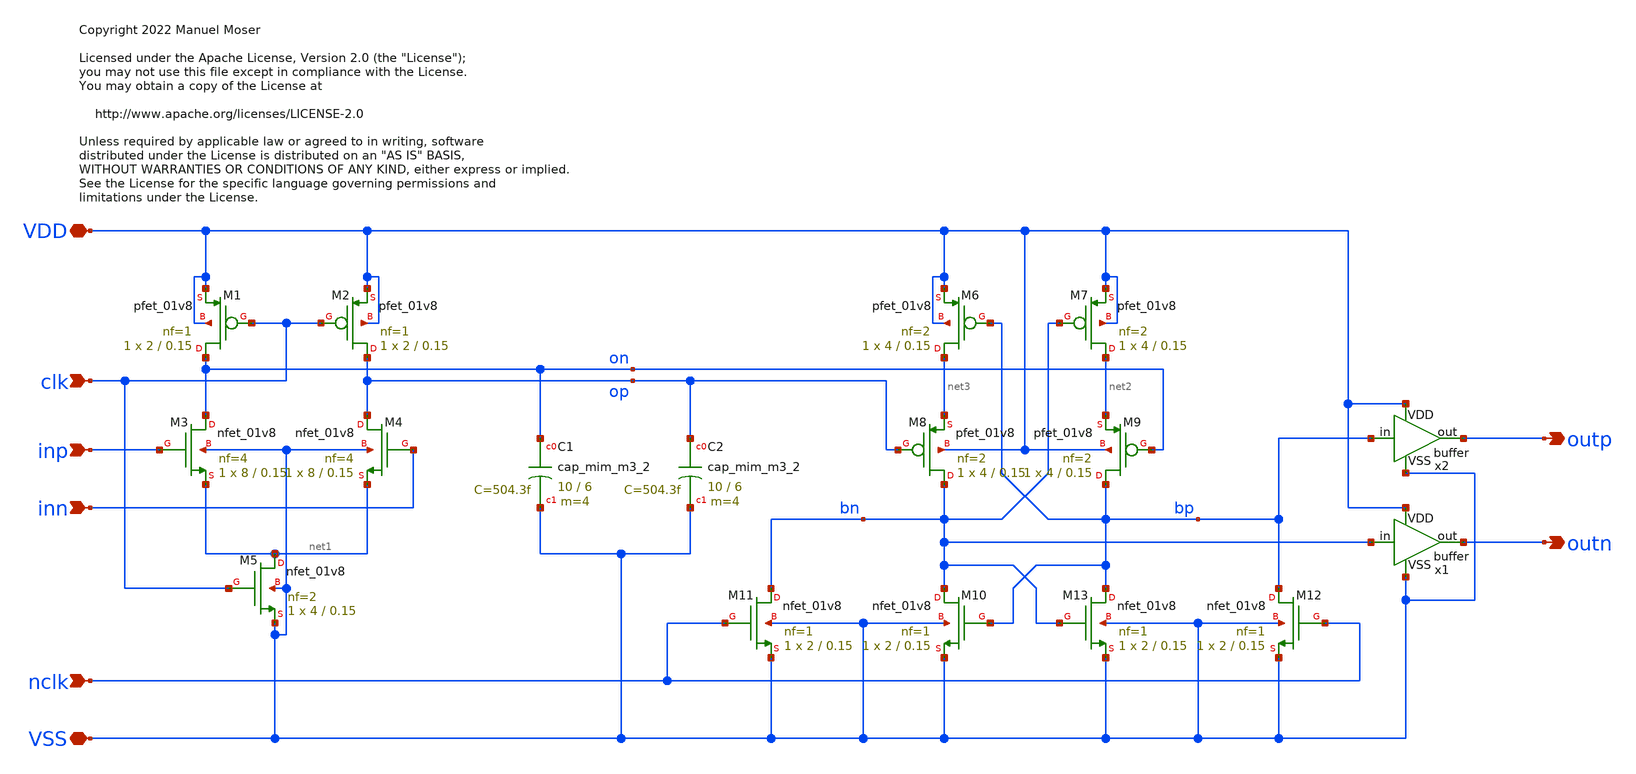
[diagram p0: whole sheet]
** sch_path: xschem/adc_comp_circuit/adc_comp_circuit.sch
* Copyright 2022 Manuel Moser
* Licensed under the Apache License, Version 2.0 (the "License");
**.subckt adc_comp_circuit VDD VSS inp inn clk nclk outp outn
*.iopin VDD
*.iopin VSS
*.ipin inp
*.ipin inn
*.ipin clk
*.ipin nclk
*.opin outp
*.opin outn
XM1 on clk VDD VDD sky130_fd_pr__pfet_01v8 L=0.15 W=2 nf=1 ad='int((nf+1)/2) * W/nf * 0.29' as='int((nf+2)/2) * W/nf * 0.29'
+ pd='2*int((nf+1)/2) * (W/nf + 0.29)' ps='2*int((nf+2)/2) * (W/nf + 0.29)' nrd='0.29 / W' nrs='0.29 / W'
+ sa=0 sb=0 sd=0 mult=1 m=1
XM2 op clk VDD VDD sky130_fd_pr__pfet_01v8 L=0.15 W=2 nf=1 ad='int((nf+1)/2) * W/nf * 0.29' as='int((nf+2)/2) * W/nf * 0.29'
+ pd='2*int((nf+1)/2) * (W/nf + 0.29)' ps='2*int((nf+2)/2) * (W/nf + 0.29)' nrd='0.29 / W' nrs='0.29 / W'
+ sa=0 sb=0 sd=0 mult=1 m=1
XM3 on inp net1 VSS sky130_fd_pr__nfet_01v8 L=0.15 W=8 nf=4 ad='int((nf+1)/2) * W/nf * 0.29' as='int((nf+2)/2) * W/nf * 0.29'
+ pd='2*int((nf+1)/2) * (W/nf + 0.29)' ps='2*int((nf+2)/2) * (W/nf + 0.29)' nrd='0.29 / W' nrs='0.29 / W'
+ sa=0 sb=0 sd=0 mult=1 m=1
XM4 op inn net1 VSS sky130_fd_pr__nfet_01v8 L=0.15 W=8 nf=4 ad='int((nf+1)/2) * W/nf * 0.29' as='int((nf+2)/2) * W/nf * 0.29'
+ pd='2*int((nf+1)/2) * (W/nf + 0.29)' ps='2*int((nf+2)/2) * (W/nf + 0.29)' nrd='0.29 / W' nrs='0.29 / W'
+ sa=0 sb=0 sd=0 mult=1 m=1
XM5 net1 clk VSS VSS sky130_fd_pr__nfet_01v8 L=0.15 W=4 nf=2 ad='int((nf+1)/2) * W/nf * 0.29' as='int((nf+2)/2) * W/nf * 0.29'
+ pd='2*int((nf+1)/2) * (W/nf + 0.29)' ps='2*int((nf+2)/2) * (W/nf + 0.29)' nrd='0.29 / W' nrs='0.29 / W'
+ sa=0 sb=0 sd=0 mult=1 m=1
XM6 net3 bp VDD VDD sky130_fd_pr__pfet_01v8 L=0.15 W=4 nf=2 ad='int((nf+1)/2) * W/nf * 0.29' as='int((nf+2)/2) * W/nf * 0.29'
+ pd='2*int((nf+1)/2) * (W/nf + 0.29)' ps='2*int((nf+2)/2) * (W/nf + 0.29)' nrd='0.29 / W' nrs='0.29 / W'
+ sa=0 sb=0 sd=0 mult=1 m=1
XM7 net2 bn VDD VDD sky130_fd_pr__pfet_01v8 L=0.15 W=4 nf=2 ad='int((nf+1)/2) * W/nf * 0.29' as='int((nf+2)/2) * W/nf * 0.29'
+ pd='2*int((nf+1)/2) * (W/nf + 0.29)' ps='2*int((nf+2)/2) * (W/nf + 0.29)' nrd='0.29 / W' nrs='0.29 / W'
+ sa=0 sb=0 sd=0 mult=1 m=1
XM8 bn op net3 VDD sky130_fd_pr__pfet_01v8 L=0.15 W=4 nf=2 ad='int((nf+1)/2) * W/nf * 0.29' as='int((nf+2)/2) * W/nf * 0.29'
+ pd='2*int((nf+1)/2) * (W/nf + 0.29)' ps='2*int((nf+2)/2) * (W/nf + 0.29)' nrd='0.29 / W' nrs='0.29 / W'
+ sa=0 sb=0 sd=0 mult=1 m=1
XM9 bp on net2 VDD sky130_fd_pr__pfet_01v8 L=0.15 W=4 nf=2 ad='int((nf+1)/2) * W/nf * 0.29' as='int((nf+2)/2) * W/nf * 0.29'
+ pd='2*int((nf+1)/2) * (W/nf + 0.29)' ps='2*int((nf+2)/2) * (W/nf + 0.29)' nrd='0.29 / W' nrs='0.29 / W'
+ sa=0 sb=0 sd=0 mult=1 m=1
XM10 bn bp VSS VSS sky130_fd_pr__nfet_01v8 L=0.15 W=2 nf=1 ad='int((nf+1)/2) * W/nf * 0.29' as='int((nf+2)/2) * W/nf * 0.29'
+ pd='2*int((nf+1)/2) * (W/nf + 0.29)' ps='2*int((nf+2)/2) * (W/nf + 0.29)' nrd='0.29 / W' nrs='0.29 / W'
+ sa=0 sb=0 sd=0 mult=1 m=1
XM11 bn nclk VSS VSS sky130_fd_pr__nfet_01v8 L=0.15 W=2 nf=1 ad='int((nf+1)/2) * W/nf * 0.29' as='int((nf+2)/2) * W/nf * 0.29'
+ pd='2*int((nf+1)/2) * (W/nf + 0.29)' ps='2*int((nf+2)/2) * (W/nf + 0.29)' nrd='0.29 / W' nrs='0.29 / W'
+ sa=0 sb=0 sd=0 mult=1 m=1
XM12 bp nclk VSS VSS sky130_fd_pr__nfet_01v8 L=0.15 W=2 nf=1 ad='int((nf+1)/2) * W/nf * 0.29' as='int((nf+2)/2) * W/nf * 0.29'
+ pd='2*int((nf+1)/2) * (W/nf + 0.29)' ps='2*int((nf+2)/2) * (W/nf + 0.29)' nrd='0.29 / W' nrs='0.29 / W'
+ sa=0 sb=0 sd=0 mult=1 m=1
XM13 bp bn VSS VSS sky130_fd_pr__nfet_01v8 L=0.15 W=2 nf=1 ad='int((nf+1)/2) * W/nf * 0.29' as='int((nf+2)/2) * W/nf * 0.29'
+ pd='2*int((nf+1)/2) * (W/nf + 0.29)' ps='2*int((nf+2)/2) * (W/nf + 0.29)' nrd='0.29 / W' nrs='0.29 / W'
+ sa=0 sb=0 sd=0 mult=1 m=1
XC1 on VSS sky130_fd_pr__cap_mim_m3_2 W=10 L=6 MF=4 m=4
XC2 op VSS sky130_fd_pr__cap_mim_m3_2 W=10 L=6 MF=4 m=4
x1 VDD bn outn VSS buffer
x2 VDD bp outp VSS buffer
**.ends
.end
